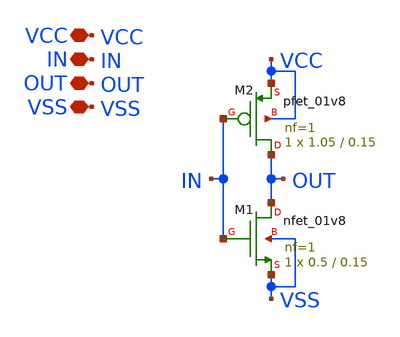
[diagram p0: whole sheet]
** sch_path: inv.sch
**.subckt inv VCC IN OUT VSS
*.iopin VCC
*.iopin IN
*.iopin OUT
*.iopin VSS
XM1 OUT IN VSS VSS sky130_fd_pr__nfet_01v8 L=0.15 W=0.5 nf=1 ad='int((nf+1)/2) * W/nf * 0.29' as='int((nf+2)/2) * W/nf * 0.29'
+ pd='2*int((nf+1)/2) * (W/nf + 0.29)' ps='2*int((nf+2)/2) * (W/nf + 0.29)' nrd='0.29 / W' nrs='0.29 / W'
+ sa=0 sb=0 sd=0 mult=1 m=1
XM2 OUT IN VCC VCC sky130_fd_pr__pfet_01v8 L=0.15 W=1.05 nf=1 ad='int((nf+1)/2) * W/nf * 0.29' as='int((nf+2)/2) * W/nf * 0.29'
+ pd='2*int((nf+1)/2) * (W/nf + 0.29)' ps='2*int((nf+2)/2) * (W/nf + 0.29)' nrd='0.29 / W' nrs='0.29 / W'
+ sa=0 sb=0 sd=0 mult=1 m=1
**.ends
.end
